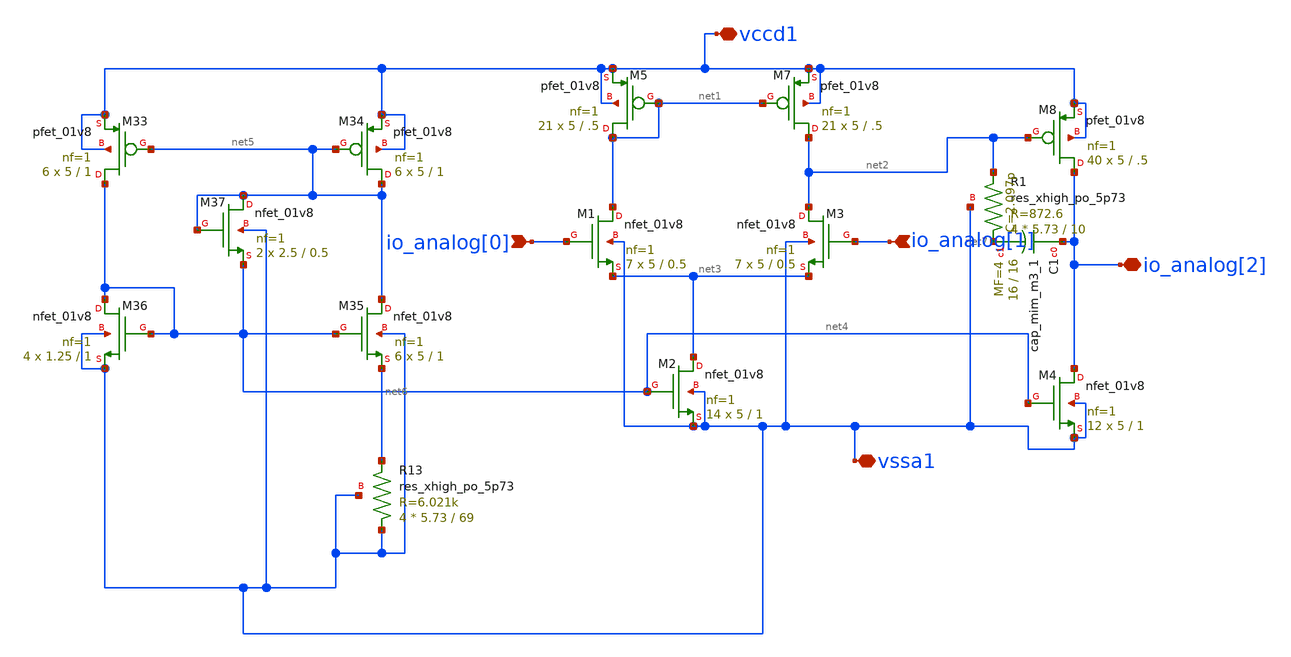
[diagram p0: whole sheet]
** sch_path: SP23_Tapeout/Tapeout_Ready_v5/OTA_GM_Schematic/OTA_MULT_GM.sch
**.subckt OTA_MULT_GM vssa1 vccd1 io_analog[0] io_analog[1] io_analog[2]
*.iopin vssa1
*.iopin vccd1
*.ipin io_analog[0]
*.ipin io_analog[1]
*.iopin io_analog[2]
XM1 net1 io_analog[0] net3 vssa1 sky130_fd_pr__nfet_01v8 L=0.5 W=5 nf=1 ad='int((nf+1)/2) * W/nf * 0.29'
+ as='int((nf+2)/2) * W/nf * 0.29' pd='2*int((nf+1)/2) * (W/nf + 0.29)' ps='2*int((nf+2)/2) * (W/nf + 0.29)'
+ nrd='0.29 / W' nrs='0.29 / W' sa=0 sb=0 sd=0 mult=7 m=7
XM2 net3 net4 vssa1 vssa1 sky130_fd_pr__nfet_01v8 L=1 W=5 nf=1 ad='int((nf+1)/2) * W/nf * 0.29' as='int((nf+2)/2) * W/nf * 0.29'
+ pd='2*int((nf+1)/2) * (W/nf + 0.29)' ps='2*int((nf+2)/2) * (W/nf + 0.29)' nrd='0.29 / W' nrs='0.29 / W'
+ sa=0 sb=0 sd=0 mult=14 m=14
XM3 net2 io_analog[1] net3 vssa1 sky130_fd_pr__nfet_01v8 L=0.5 W=5 nf=1 ad='int((nf+1)/2) * W/nf * 0.29'
+ as='int((nf+2)/2) * W/nf * 0.29' pd='2*int((nf+1)/2) * (W/nf + 0.29)' ps='2*int((nf+2)/2) * (W/nf + 0.29)'
+ nrd='0.29 / W' nrs='0.29 / W' sa=0 sb=0 sd=0 mult=7 m=7
XM4 io_analog[2] net4 vssa1 vssa1 sky130_fd_pr__nfet_01v8 L=1 W=5 nf=1 ad='int((nf+1)/2) * W/nf * 0.29'
+ as='int((nf+2)/2) * W/nf * 0.29' pd='2*int((nf+1)/2) * (W/nf + 0.29)' ps='2*int((nf+2)/2) * (W/nf + 0.29)'
+ nrd='0.29 / W' nrs='0.29 / W' sa=0 sb=0 sd=0 mult=12 m=12
XM5 net1 net1 vccd1 vccd1 sky130_fd_pr__pfet_01v8 L=.5 W=5 nf=1 ad='int((nf+1)/2) * W/nf * 0.29' as='int((nf+2)/2) * W/nf * 0.29'
+ pd='2*int((nf+1)/2) * (W/nf + 0.29)' ps='2*int((nf+2)/2) * (W/nf + 0.29)' nrd='0.29 / W' nrs='0.29 / W'
+ sa=0 sb=0 sd=0 mult=21 m=21
XM7 net2 net1 vccd1 vccd1 sky130_fd_pr__pfet_01v8 L=.5 W=5 nf=1 ad='int((nf+1)/2) * W/nf * 0.29' as='int((nf+2)/2) * W/nf * 0.29'
+ pd='2*int((nf+1)/2) * (W/nf + 0.29)' ps='2*int((nf+2)/2) * (W/nf + 0.29)' nrd='0.29 / W' nrs='0.29 / W'
+ sa=0 sb=0 sd=0 mult=21 m=21
XM8 io_analog[2] net2 vccd1 vccd1 sky130_fd_pr__pfet_01v8 L=.5 W=5 nf=1 ad='int((nf+1)/2) * W/nf * 0.29'
+ as='int((nf+2)/2) * W/nf * 0.29' pd='2*int((nf+1)/2) * (W/nf + 0.29)' ps='2*int((nf+2)/2) * (W/nf + 0.29)'
+ nrd='0.29 / W' nrs='0.29 / W' sa=0 sb=0 sd=0 mult=40 m=40
XR1 net7 net2 vssa1 sky130_fd_pr__res_xhigh_po_5p73 L=10 mult=4 m=4
XC1 io_analog[2] net7 sky130_fd_pr__cap_mim_m3_1 W=16 L=16 MF=4 m=4
XM33 net4 net5 vccd1 vccd1 sky130_fd_pr__pfet_01v8 L=1 W=5 nf=1 ad='int((nf+1)/2) * W/nf * 0.29' as='int((nf+2)/2) * W/nf * 0.29'
+ pd='2*int((nf+1)/2) * (W/nf + 0.29)' ps='2*int((nf+2)/2) * (W/nf + 0.29)' nrd='0.29 / W' nrs='0.29 / W'
+ sa=0 sb=0 sd=0 mult=6 m=6
XM34 net5 net5 vccd1 vccd1 sky130_fd_pr__pfet_01v8 L=1 W=5 nf=1 ad='int((nf+1)/2) * W/nf * 0.29' as='int((nf+2)/2) * W/nf * 0.29'
+ pd='2*int((nf+1)/2) * (W/nf + 0.29)' ps='2*int((nf+2)/2) * (W/nf + 0.29)' nrd='0.29 / W' nrs='0.29 / W'
+ sa=0 sb=0 sd=0 mult=6 m=6
XM35 net5 net4 net6 vssa1 sky130_fd_pr__nfet_01v8 L=1 W=5 nf=1 ad='int((nf+1)/2) * W/nf * 0.29' as='int((nf+2)/2) * W/nf * 0.29'
+ pd='2*int((nf+1)/2) * (W/nf + 0.29)' ps='2*int((nf+2)/2) * (W/nf + 0.29)' nrd='0.29 / W' nrs='0.29 / W'
+ sa=0 sb=0 sd=0 mult=6 m=6
XM36 net4 net4 vssa1 vssa1 sky130_fd_pr__nfet_01v8 L=1 W=1.25 nf=1 ad='int((nf+1)/2) * W/nf * 0.29' as='int((nf+2)/2) * W/nf * 0.29'
+ pd='2*int((nf+1)/2) * (W/nf + 0.29)' ps='2*int((nf+2)/2) * (W/nf + 0.29)' nrd='0.29 / W' nrs='0.29 / W'
+ sa=0 sb=0 sd=0 mult=4 m=4
XM37 net5 net5 net4 vssa1 sky130_fd_pr__nfet_01v8 L=0.5 W=2.5 nf=1 ad='int((nf+1)/2) * W/nf * 0.29' as='int((nf+2)/2) * W/nf * 0.29'
+ pd='2*int((nf+1)/2) * (W/nf + 0.29)' ps='2*int((nf+2)/2) * (W/nf + 0.29)' nrd='0.29 / W' nrs='0.29 / W'
+ sa=0 sb=0 sd=0 mult=2 m=2
XR13 vssa1 net6 vssa1 sky130_fd_pr__res_xhigh_po_5p73 L=69 mult=4 m=4
**.ends
.end
